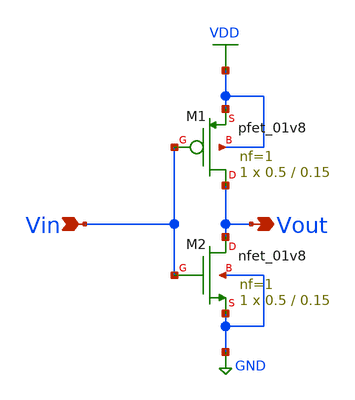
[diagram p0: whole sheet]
** sch_path: mux_xshcem/inverter.sch
**.subckt inverter Vin Vout
*.ipin Vin
*.opin Vout
XM1 Vout Vin VDD VDD sky130_fd_pr__pfet_01v8 L=0.15 W=0.5 nf=1 ad='int((1 + 1)/2) * 0.5 / 1 * 0.29' as='int((1 + 2)/2) * 0.5 / 1 * 0.29'
+ pd='2*int((1 + 1)/2) * (0.5 / 1 + 0.29)' ps='2*int((1 + 2)/2) * (0.5 / 1 + 0.29)' nrd='0.29 / 0.5 ' nrs='0.29 / 0.5 '
+ sa=0 sb=0 sd=0 mult=1 m=1
XM2 Vout Vin GND GND sky130_fd_pr__nfet_01v8 L=0.15 W=0.5 nf=1 ad='int((1 + 1)/2) * 0.5 / 1 * 0.29' as='int((1 + 2)/2) * 0.5 / 1 * 0.29'
+ pd='2*int((1 + 1)/2) * (0.5 / 1 + 0.29)' ps='2*int((1 + 2)/2) * (0.5 / 1 + 0.29)' nrd='0.29 / 0.5 ' nrs='0.29 / 0.5 '
+ sa=0 sb=0 sd=0 mult=1 m=1
**.ends
.GLOBAL VDD
.GLOBAL GND
.end
